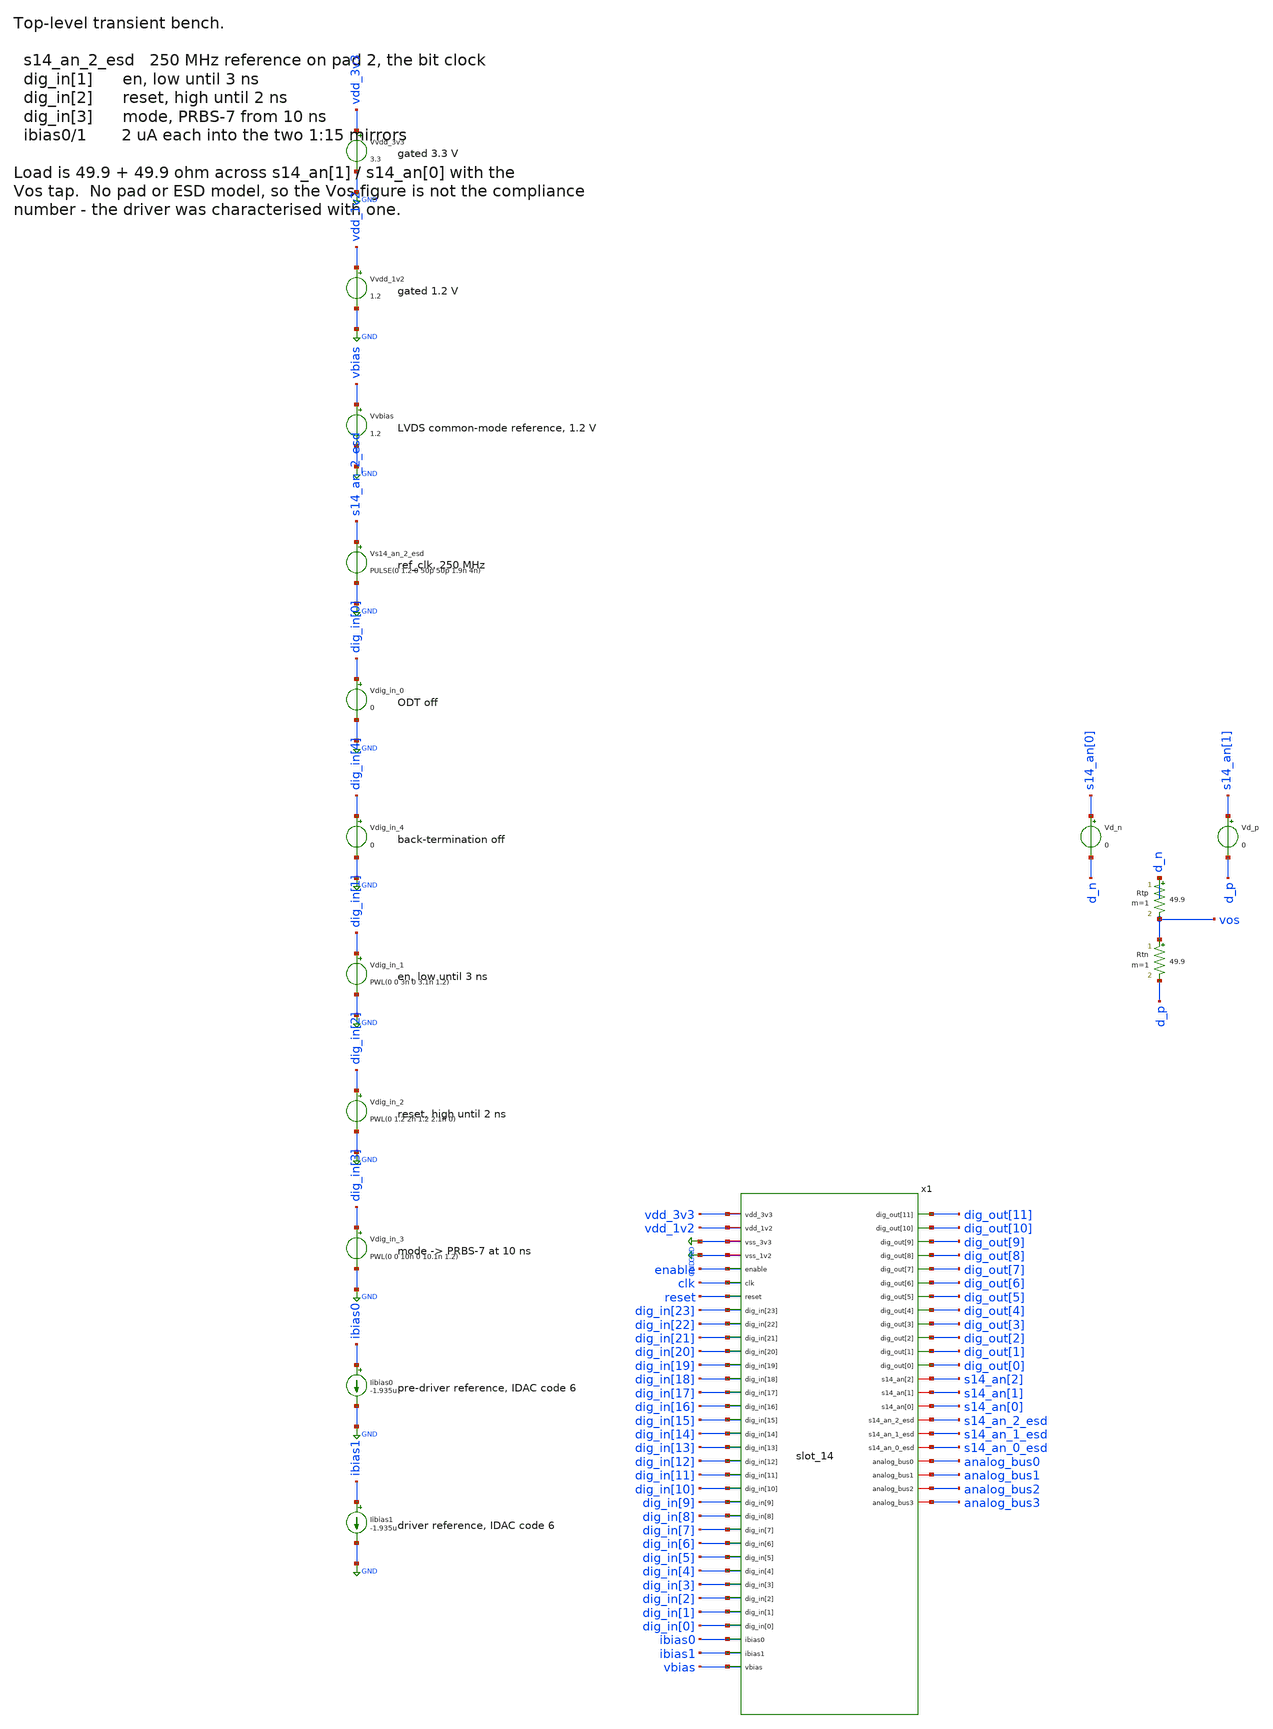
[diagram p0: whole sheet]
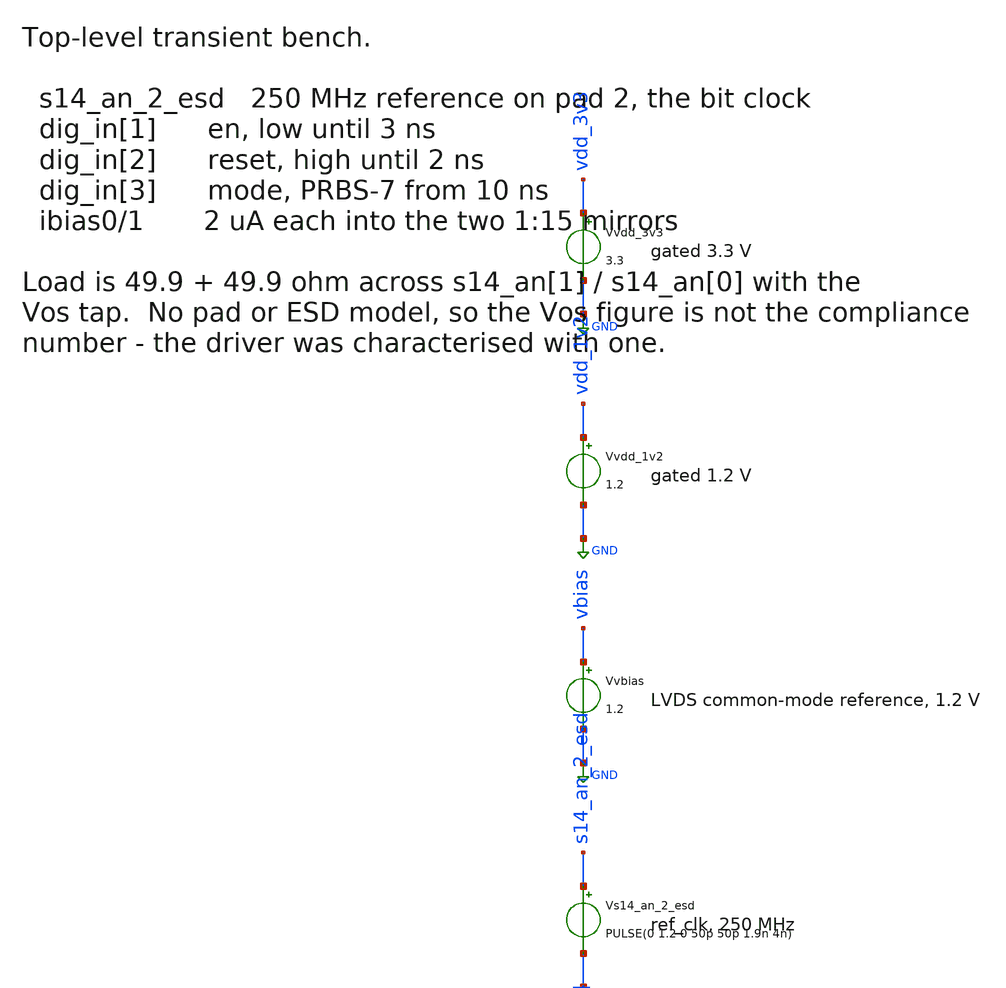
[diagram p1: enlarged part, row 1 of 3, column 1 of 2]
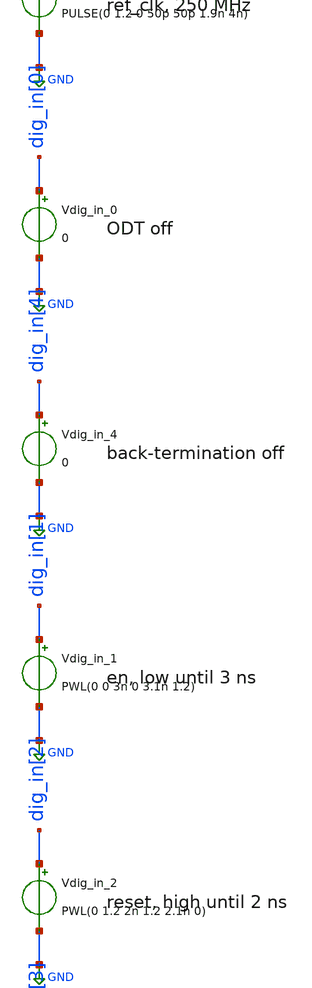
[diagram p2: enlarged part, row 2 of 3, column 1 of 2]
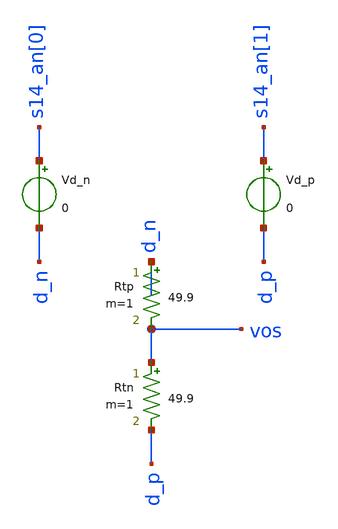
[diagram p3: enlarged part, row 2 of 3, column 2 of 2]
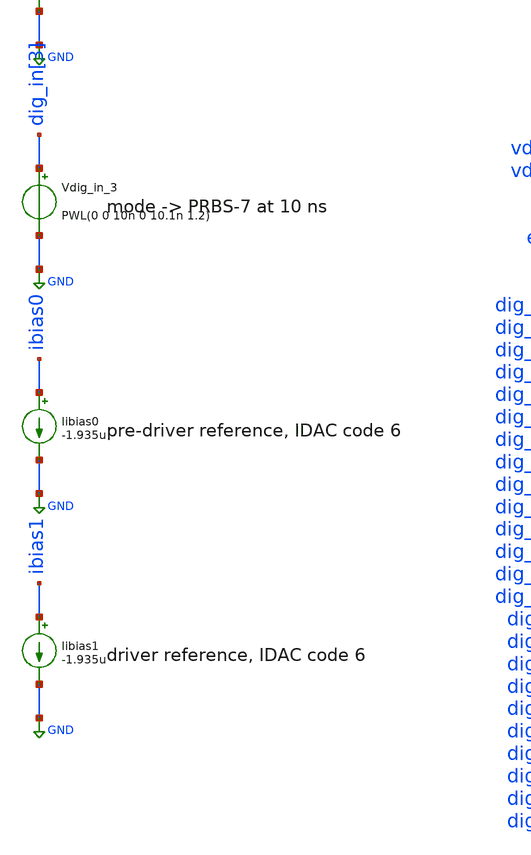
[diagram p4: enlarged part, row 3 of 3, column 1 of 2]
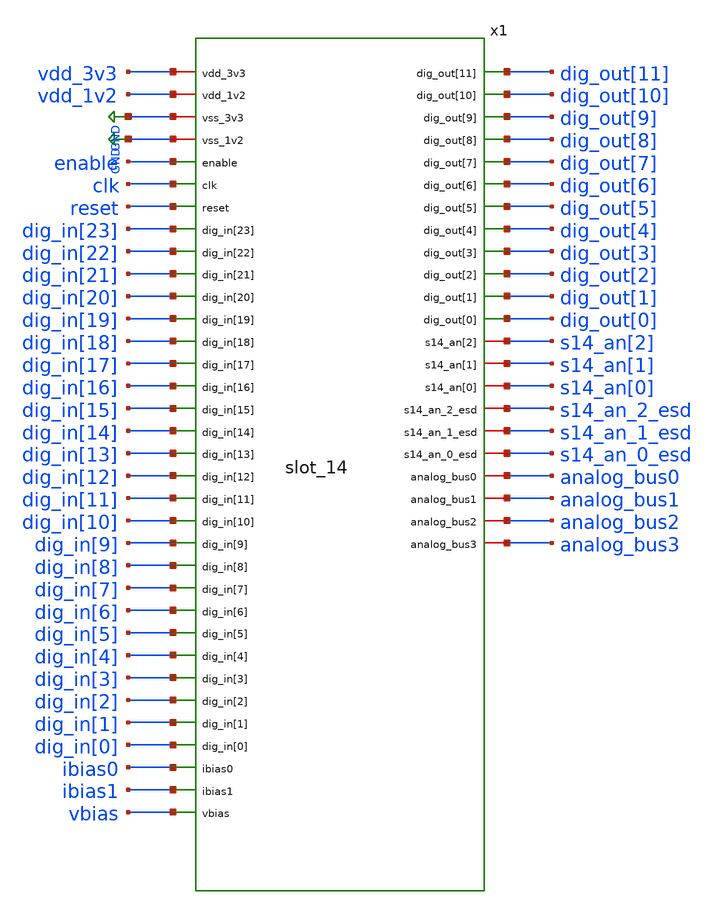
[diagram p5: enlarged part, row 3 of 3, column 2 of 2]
** sch_path: testbenches/xschem/slot_14_tb_tran.sch
**.subckt slot_14_tb_tran
Vvdd_3v3 vdd_3v3 GND 3.3
Vvdd_1v2 vdd_1v2 GND 1.2
Vvbias vbias GND 1.2
Vs14_an_2_esd s14_an_2_esd GND PULSE(0 1.2 0 50p 50p 1.9n 4n)
Vdig_in_0 dig_in[0] GND 0
Vdig_in_4 dig_in[4] GND 0
Vdig_in_1 dig_in[1] GND PWL(0 0 3n 0 3.1n 1.2)
Vdig_in_2 dig_in[2] GND PWL(0 1.2 2n 1.2 2.1n 0)
Vdig_in_3 dig_in[3] GND PWL(0 0 10n 0 10.1n 1.2)
Iibias0 ibias0 GND -1.935u
Iibias1 ibias1 GND -1.935u
x1 vdd_3v3 vdd_1v2 GND GND enable clk reset dig_in[23] dig_in[22] dig_in[21] dig_in[20] dig_in[19]
+ dig_in[18] dig_in[17] dig_in[16] dig_in[15] dig_in[14] dig_in[13] dig_in[12] dig_in[11] dig_in[10] dig_in[9]
+ dig_in[8] dig_in[7] dig_in[6] dig_in[5] dig_in[4] dig_in[3] dig_in[2] dig_in[1] dig_in[0] ibias0 ibias1 vbias
+ dig_out[11] dig_out[10] dig_out[9] dig_out[8] dig_out[7] dig_out[6] dig_out[5] dig_out[4] dig_out[3] dig_out[2]
+ dig_out[1] dig_out[0] s14_an[2] s14_an[1] s14_an[0] s14_an_2_esd s14_an_1_esd s14_an_0_esd analog_bus0
+ analog_bus1 analog_bus2 analog_bus3 slot_14
Vd_n s14_an[0] d_n 0
Vd_p s14_an[1] d_p 0
Rtp d_n vos 49.9 m=1
Rtn vos d_p 49.9 m=1
**** begin user architecture code


.lib cornerMOSlv.lib mos_tt
.lib cornerMOShv.lib mos_tt
.lib cornerRES.lib res_typ
.include ../../../models/diodes_tt0.lib
.include sg13g2_esd.lib
.include cap_cmomf.lib
.include /foss/pdks/ihp-sg13cmos5l/libs.ref/sg13cmos5l_stdcell/spice/sg13cmos5l_stdcell.spice
.temp 27
.options savecurrents klu method=trap reltol=1e-3 abstol=1e-12 gmin=1e-12
.ic v(x1.xlvds.xdrv.cmfb)=1.54
.control
save all
op
remzerovec
write @schname\.raw
set appendwrite
tran 5p 40n
write @schname\.raw

let vod = v(d_p)-v(d_n)
meas tran vod_max MAX vod from=20n to=40n
meas tran vod_min MIN vod from=20n to=40n
meas tran vos_avg AVG v(vos) from=20n to=40n
meas tran vos_max MAX v(vos) from=20n to=40n
meas tran vos_min MIN v(vos) from=20n to=40n
let vos_pp = vos_max - vos_min
print vod_max vod_min vos_avg vos_pp

set wr_vecnames
set wr_singlescale
wrdata ../plot_simulations/data/@schname\.txt  v(d_p) v(d_n) v(vos) vod v(x1.core_p) v(x1.core_n)
.endc


**** end user architecture code
**.ends
.GLOBAL GND
.end
